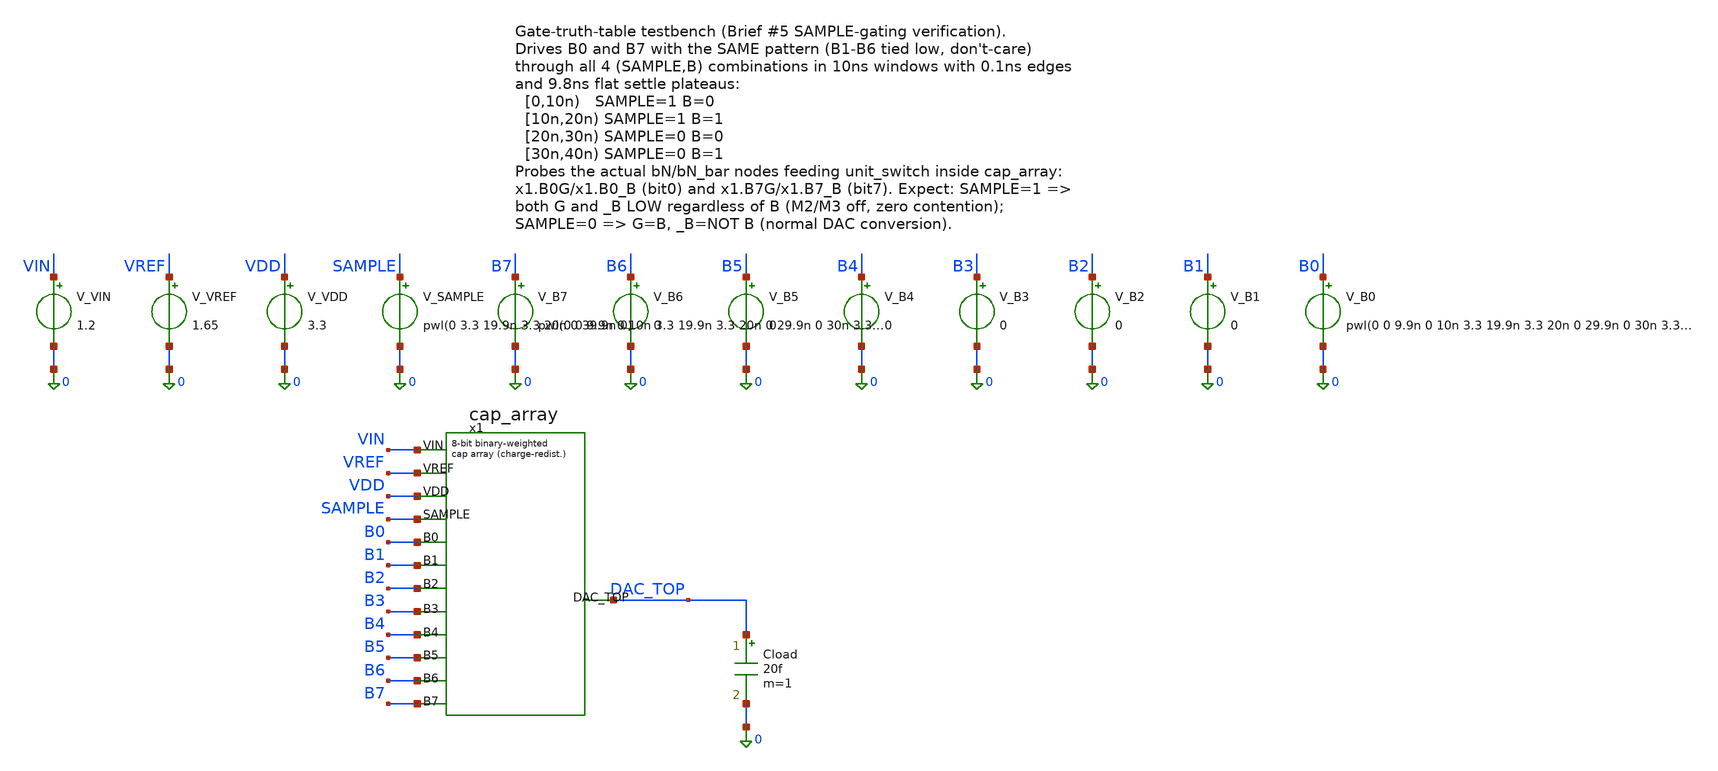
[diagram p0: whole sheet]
** sch_path: dac/sim/tb_gate_truth.sch
**.subckt tb_gate_truth
V_VIN VIN 0 1.2
V_VREF VREF 0 1.65
V_VDD VDD 0 3.3
V_SAMPLE SAMPLE 0 pwl(0 3.3 19.9n 3.3 20n 0 39.9n 0)
V_B7 B7 0 pwl(0 0 9.9n 0 10n 3.3 19.9n 3.3 20n 0 29.9n 0 30n 3.3 39.9n 3.3)
V_B6 B6 0 0
V_B5 B5 0 0
V_B4 B4 0 0
V_B3 B3 0 0
V_B2 B2 0 0
V_B1 B1 0 0
V_B0 B0 0 pwl(0 0 9.9n 0 10n 3.3 19.9n 3.3 20n 0 29.9n 0 30n 3.3 39.9n 3.3)
Cload DAC_TOP 0 20f m=1
x1 VIN VREF VDD SAMPLE B0 B1 B2 B3 B4 B5 B6 B7 DAC_TOP cap_array
**** begin user architecture code


.param nfet_wid=0.42u nfet_len=0.28u
.param mim_corner_1p0fF=1 mim_corner_1p5fF=1 mim_corner_2p0fF=1
.param mc_c_cox_1p0fF=0 mc_c_cox_1p5fF=0 mc_c_cox_2p0fF=0
.param var_vth=0 var_k=0
.lib /foss/pdks/gf180mcuD/libs.tech/ngspice/sm141064.ngspice typical
.lib /foss/pdks/gf180mcuD/libs.tech/ngspice/sm141064.ngspice cap_mim
.include /foss/pdks/gf180mcuD/libs.tech/ngspice/design.ngspice
.options savecurrents
.control
save all
tran 0.01n 40n
* bit0 truth table
meas tran b0g_s1_b0 FIND v(x1.B0G) AT=5n
meas tran b0b_s1_b0 FIND v(x1.B0_B) AT=5n
meas tran b0g_s1_b1 FIND v(x1.B0G) AT=15n
meas tran b0b_s1_b1 FIND v(x1.B0_B) AT=15n
meas tran b0g_s0_b0 FIND v(x1.B0G) AT=25n
meas tran b0b_s0_b0 FIND v(x1.B0_B) AT=25n
meas tran b0g_s0_b1 FIND v(x1.B0G) AT=35n
meas tran b0b_s0_b1 FIND v(x1.B0_B) AT=35n
* bit7 truth table
meas tran b7g_s1_b0 FIND v(x1.B7G) AT=5n
meas tran b7b_s1_b0 FIND v(x1.B7_B) AT=5n
meas tran b7g_s1_b1 FIND v(x1.B7G) AT=15n
meas tran b7b_s1_b1 FIND v(x1.B7_B) AT=15n
meas tran b7g_s0_b0 FIND v(x1.B7G) AT=25n
meas tran b7b_s0_b0 FIND v(x1.B7_B) AT=25n
meas tran b7g_s0_b1 FIND v(x1.B7G) AT=35n
meas tran b7b_s0_b1 FIND v(x1.B7_B) AT=35n
echo bit0_truth_table_V:
print b0g_s1_b0 b0b_s1_b0 b0g_s1_b1 b0b_s1_b1 b0g_s0_b0 b0b_s0_b0 b0g_s0_b1 b0b_s0_b1
echo bit7_truth_table_V:
print b7g_s1_b0 b7b_s1_b0 b7g_s1_b1 b7b_s1_b1 b7g_s0_b0 b7b_s0_b0 b7g_s0_b1 b7b_s0_b1
.endc


**** end user architecture code
**.ends
.end
